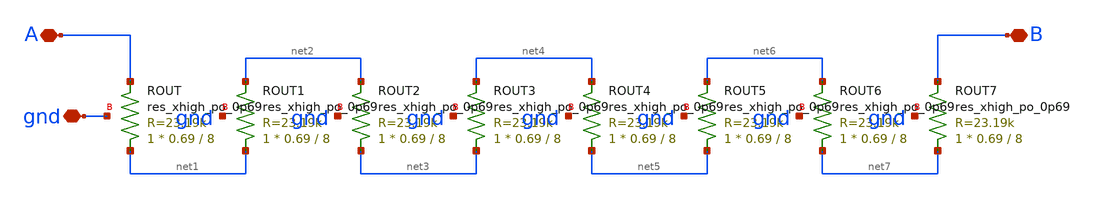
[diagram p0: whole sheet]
** sch_path: xschem/rev_1/rout_185k_high_po.sch
**.subckt rout_185k_high_po A B gnd
*.iopin A
*.iopin B
*.iopin gnd
XROUT net1 A gnd sky130_fd_pr__res_xhigh_po_0p69 L=8 mult=1 m=1
XROUT1 net1 net2 gnd sky130_fd_pr__res_xhigh_po_0p69 L=8 mult=1 m=1
XROUT2 net3 net2 gnd sky130_fd_pr__res_xhigh_po_0p69 L=8 mult=1 m=1
XROUT3 net3 net4 gnd sky130_fd_pr__res_xhigh_po_0p69 L=8 mult=1 m=1
XROUT4 net5 net4 gnd sky130_fd_pr__res_xhigh_po_0p69 L=8 mult=1 m=1
XROUT5 net5 net6 gnd sky130_fd_pr__res_xhigh_po_0p69 L=8 mult=1 m=1
XROUT6 net7 net6 gnd sky130_fd_pr__res_xhigh_po_0p69 L=8 mult=1 m=1
XROUT7 net7 B gnd sky130_fd_pr__res_xhigh_po_0p69 L=8 mult=1 m=1
**.ends
.end
